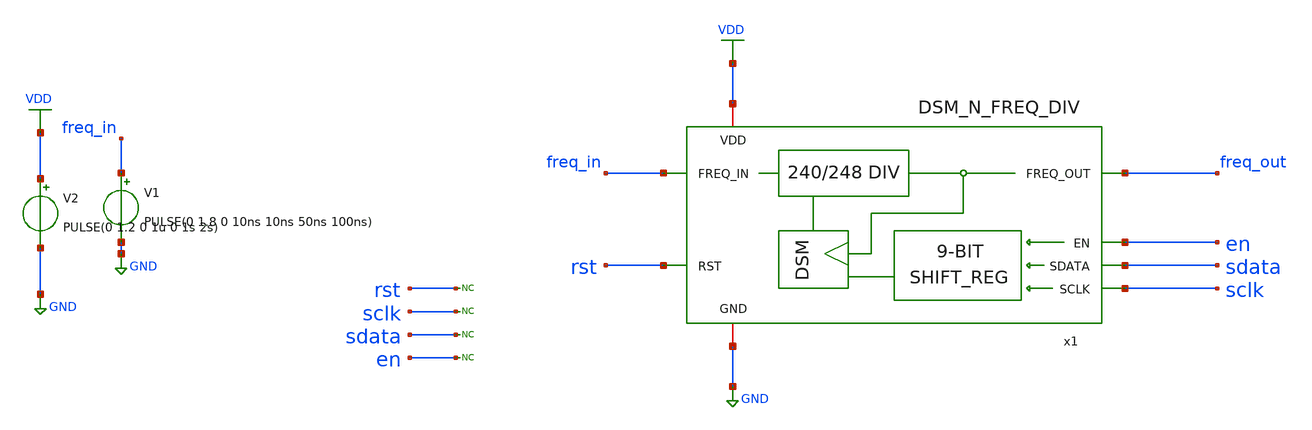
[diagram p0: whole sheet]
** sch_path: xschem/dsm/xschem/tb_DSM_N_FREQ_DIV_PEX.sch
* Copyright (C) 1998-2024 Stefan Frederik Schippers
* This program is free software; you can redistribute it and/or modify
* it under the terms of the GNU General Public License as published by
* the Free Software Foundation; either version 2 of the License, or
* (at your option) any later version.
* This program is distributed in the hope that it will be useful,
* but WITHOUT ANY WARRANTY; without even the implied warranty of
* MERCHANTABILITY or FITNESS FOR A PARTICULAR PURPOSE.  See the
* GNU General Public License for more details.
* You should have received a copy of the GNU General Public License
* along with this program; if not, write to the Free Software
**.subckt tb_DSM_N_FREQ_DIV_PEX
V1 freq_in GND PULSE(0 1.8 0 10ns 10ns 50ns 100ns)
* noconn rst
* noconn sclk
* noconn sdata
* noconn en
V2 VDD GND PULSE(0 1.2 0 1u 0 1s 2s)
x1 [ freq_in rst sclk sdata en ] [ freq_out ] null dut
.model dut d_cosim simulation=../simulations/dsm_and_freq_divider.so
**** begin user architecture code



* ngspice commands
.save v(dout) v(sdata) v(sclk) v(en) v(rst) v(dsm_clk) v(freq_in) v(freq_out)
.control
  tran 0.5n 1m
  remzerovec
  write tb_DSM_N_FREQ_DIV_PEX.raw
.endc

* to generate following file copy stimuli.test
* to the simulation directory and run simulation -> Utile Stimuli Editor (GUI),
* and press 'Translate'
.include stimuli_test.cir




.include /foss/designs/unicasss-tools/frac-n-pll-vco-unic_cass/pex/DSM_N_FREQ_DIV__DSM_N_FREQ_DIV/magic_RC/DSM_N_FREQ_DIV.pex.spice
.lib cornerMOSlv.lib mos_tt
.lib cornerMOShv.lib mos_tt
.lib cornerRES.lib res_typ
.lib cornerCAP.lib cap_typ

**** end user architecture code
**.ends
.GLOBAL GND
.GLOBAL VDD
.end
